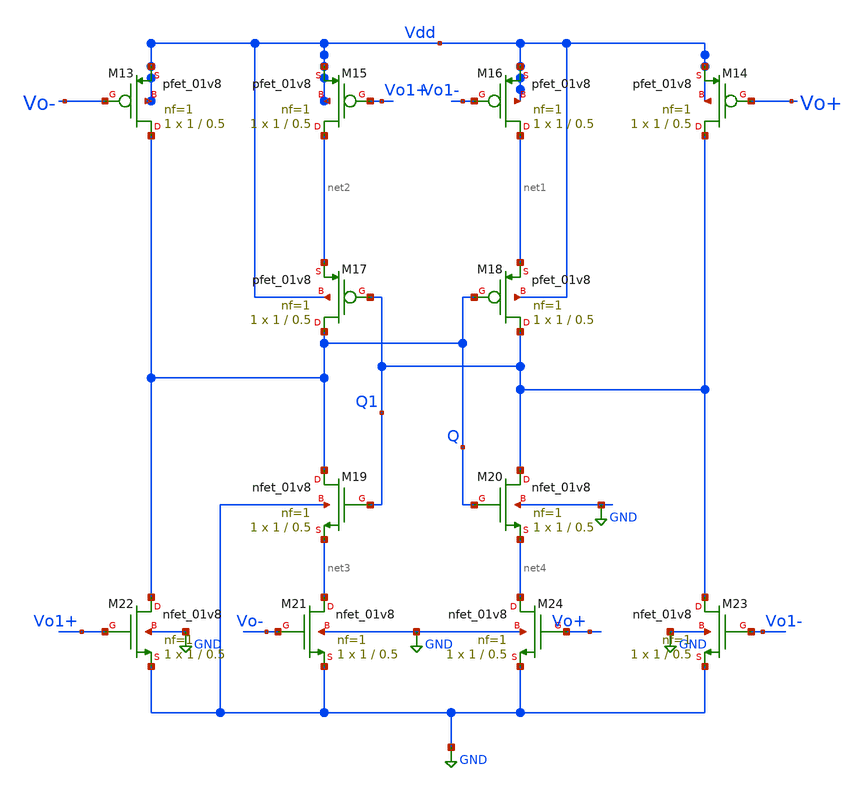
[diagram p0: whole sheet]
** sch_path: xschem/xschemfiles/latch_layout.sch
**.subckt latch_layout
XM13 Q Vo- Vdd Vdd sky130_fd_pr__pfet_01v8 L=0.5 W=1 nf=1 ad='int((nf+1)/2) * W/nf * 0.29' as='int((nf+2)/2) * W/nf * 0.29'
+ pd='2*int((nf+1)/2) * (W/nf + 0.29)' ps='2*int((nf+2)/2) * (W/nf + 0.29)' nrd='0.29 / W' nrs='0.29 / W'
+ sa=0 sb=0 sd=0 mult=1 m=1
XM14 Q1 Vo+ Vdd Vdd sky130_fd_pr__pfet_01v8 L=0.5 W=1 nf=1 ad='int((nf+1)/2) * W/nf * 0.29' as='int((nf+2)/2) * W/nf * 0.29'
+ pd='2*int((nf+1)/2) * (W/nf + 0.29)' ps='2*int((nf+2)/2) * (W/nf + 0.29)' nrd='0.29 / W' nrs='0.29 / W'
+ sa=0 sb=0 sd=0 mult=1 m=1
XM15 net2 Vo1+ Vdd Vdd sky130_fd_pr__pfet_01v8 L=0.5 W=1 nf=1 ad='int((nf+1)/2) * W/nf * 0.29' as='int((nf+2)/2) * W/nf * 0.29'
+ pd='2*int((nf+1)/2) * (W/nf + 0.29)' ps='2*int((nf+2)/2) * (W/nf + 0.29)' nrd='0.29 / W' nrs='0.29 / W'
+ sa=0 sb=0 sd=0 mult=1 m=1
XM16 net1 Vo1- Vdd Vdd sky130_fd_pr__pfet_01v8 L=0.5 W=1 nf=1 ad='int((nf+1)/2) * W/nf * 0.29' as='int((nf+2)/2) * W/nf * 0.29'
+ pd='2*int((nf+1)/2) * (W/nf + 0.29)' ps='2*int((nf+2)/2) * (W/nf + 0.29)' nrd='0.29 / W' nrs='0.29 / W'
+ sa=0 sb=0 sd=0 mult=1 m=1
XM17 Q Q1 net2 Vdd sky130_fd_pr__pfet_01v8 L=0.5 W=1 nf=1 ad='int((nf+1)/2) * W/nf * 0.29' as='int((nf+2)/2) * W/nf * 0.29'
+ pd='2*int((nf+1)/2) * (W/nf + 0.29)' ps='2*int((nf+2)/2) * (W/nf + 0.29)' nrd='0.29 / W' nrs='0.29 / W'
+ sa=0 sb=0 sd=0 mult=1 m=1
XM18 Q1 Q net1 Vdd sky130_fd_pr__pfet_01v8 L=0.5 W=1 nf=1 ad='int((nf+1)/2) * W/nf * 0.29' as='int((nf+2)/2) * W/nf * 0.29'
+ pd='2*int((nf+1)/2) * (W/nf + 0.29)' ps='2*int((nf+2)/2) * (W/nf + 0.29)' nrd='0.29 / W' nrs='0.29 / W'
+ sa=0 sb=0 sd=0 mult=1 m=1
XM19 Q Q1 net3 GND sky130_fd_pr__nfet_01v8 L=0.5 W=1 nf=1 ad='int((nf+1)/2) * W/nf * 0.29' as='int((nf+2)/2) * W/nf * 0.29'
+ pd='2*int((nf+1)/2) * (W/nf + 0.29)' ps='2*int((nf+2)/2) * (W/nf + 0.29)' nrd='0.29 / W' nrs='0.29 / W'
+ sa=0 sb=0 sd=0 mult=1 m=1
XM20 Q1 Q net4 GND sky130_fd_pr__nfet_01v8 L=0.5 W=1 nf=1 ad='int((nf+1)/2) * W/nf * 0.29' as='int((nf+2)/2) * W/nf * 0.29'
+ pd='2*int((nf+1)/2) * (W/nf + 0.29)' ps='2*int((nf+2)/2) * (W/nf + 0.29)' nrd='0.29 / W' nrs='0.29 / W'
+ sa=0 sb=0 sd=0 mult=1 m=1
XM21 net3 Vo- GND GND sky130_fd_pr__nfet_01v8 L=0.5 W=1 nf=1 ad='int((nf+1)/2) * W/nf * 0.29' as='int((nf+2)/2) * W/nf * 0.29'
+ pd='2*int((nf+1)/2) * (W/nf + 0.29)' ps='2*int((nf+2)/2) * (W/nf + 0.29)' nrd='0.29 / W' nrs='0.29 / W'
+ sa=0 sb=0 sd=0 mult=1 m=1
XM22 Q Vo1+ GND GND sky130_fd_pr__nfet_01v8 L=0.5 W=1 nf=1 ad='int((nf+1)/2) * W/nf * 0.29' as='int((nf+2)/2) * W/nf * 0.29'
+ pd='2*int((nf+1)/2) * (W/nf + 0.29)' ps='2*int((nf+2)/2) * (W/nf + 0.29)' nrd='0.29 / W' nrs='0.29 / W'
+ sa=0 sb=0 sd=0 mult=1 m=1
XM23 Q1 Vo1- GND GND sky130_fd_pr__nfet_01v8 L=0.5 W=1 nf=1 ad='int((nf+1)/2) * W/nf * 0.29' as='int((nf+2)/2) * W/nf * 0.29'
+ pd='2*int((nf+1)/2) * (W/nf + 0.29)' ps='2*int((nf+2)/2) * (W/nf + 0.29)' nrd='0.29 / W' nrs='0.29 / W'
+ sa=0 sb=0 sd=0 mult=1 m=1
XM24 net4 Vo+ GND GND sky130_fd_pr__nfet_01v8 L=0.5 W=1 nf=1 ad='int((nf+1)/2) * W/nf * 0.29' as='int((nf+2)/2) * W/nf * 0.29'
+ pd='2*int((nf+1)/2) * (W/nf + 0.29)' ps='2*int((nf+2)/2) * (W/nf + 0.29)' nrd='0.29 / W' nrs='0.29 / W'
+ sa=0 sb=0 sd=0 mult=1 m=1
**.ends
.GLOBAL GND
.end
